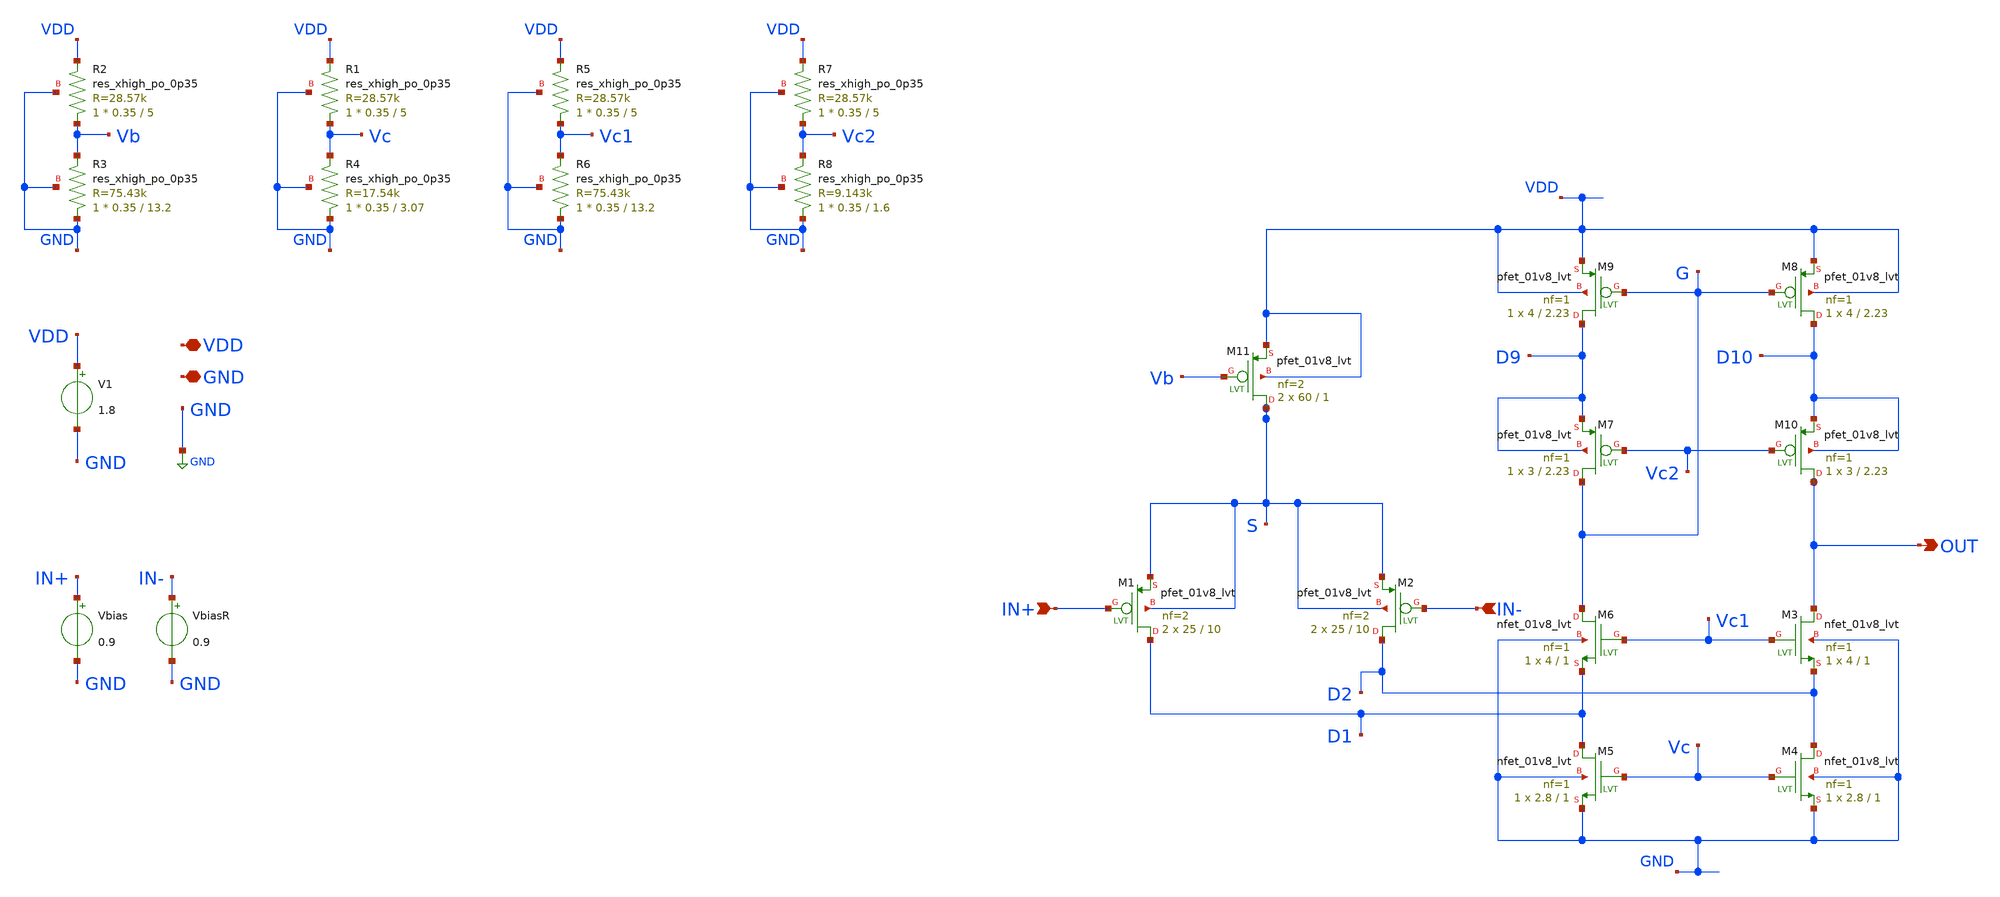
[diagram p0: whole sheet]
** sch_path: xschem/untitled-4.sch
**.subckt untitled-4 VDD GND IN+ IN- OUT
*.iopin VDD
*.iopin GND
*.ipin IN+
*.ipin IN-
*.opin OUT
V1 VDD GND 1.8
Vbias IN+ GND 0.9
XM11 S Vb VDD VDD sky130_fd_pr__pfet_01v8_lvt L=1 W=60 nf=2 ad='int((nf+1)/2) * W/nf * 0.29' as='int((nf+2)/2) * W/nf * 0.29'
+ pd='2*int((nf+1)/2) * (W/nf + 0.29)' ps='2*int((nf+2)/2) * (W/nf + 0.29)' nrd='0.29 / W' nrs='0.29 / W'
+ sa=0 sb=0 sd=0 mult=2 m=2
XM1 D1 IN+ S S sky130_fd_pr__pfet_01v8_lvt L=10 W=25 nf=2 ad='int((nf+1)/2) * W/nf * 0.29' as='int((nf+2)/2) * W/nf * 0.29'
+ pd='2*int((nf+1)/2) * (W/nf + 0.29)' ps='2*int((nf+2)/2) * (W/nf + 0.29)' nrd='0.29 / W' nrs='0.29 / W'
+ sa=0 sb=0 sd=0 mult=2 m=2
XM2 D2 IN- S S sky130_fd_pr__pfet_01v8_lvt L=10 W=25 nf=2 ad='int((nf+1)/2) * W/nf * 0.29' as='int((nf+2)/2) * W/nf * 0.29'
+ pd='2*int((nf+1)/2) * (W/nf + 0.29)' ps='2*int((nf+2)/2) * (W/nf + 0.29)' nrd='0.29 / W' nrs='0.29 / W'
+ sa=0 sb=0 sd=0 mult=2 m=2
XM3 OUT Vc1 D2 GND sky130_fd_pr__nfet_01v8_lvt L=1 W=4 nf=1 ad='int((nf+1)/2) * W/nf * 0.29' as='int((nf+2)/2) * W/nf * 0.29'
+ pd='2*int((nf+1)/2) * (W/nf + 0.29)' ps='2*int((nf+2)/2) * (W/nf + 0.29)' nrd='0.29 / W' nrs='0.29 / W'
+ sa=0 sb=0 sd=0 mult=1 m=1
XM4 D2 Vc GND GND sky130_fd_pr__nfet_01v8_lvt L=1 W=2.8 nf=1 ad='int((nf+1)/2) * W/nf * 0.29' as='int((nf+2)/2) * W/nf * 0.29'
+ pd='2*int((nf+1)/2) * (W/nf + 0.29)' ps='2*int((nf+2)/2) * (W/nf + 0.29)' nrd='0.29 / W' nrs='0.29 / W'
+ sa=0 sb=0 sd=0 mult=1 m=1
XM5 D1 Vc GND GND sky130_fd_pr__nfet_01v8_lvt L=1 W=2.8 nf=1 ad='int((nf+1)/2) * W/nf * 0.29' as='int((nf+2)/2) * W/nf * 0.29'
+ pd='2*int((nf+1)/2) * (W/nf + 0.29)' ps='2*int((nf+2)/2) * (W/nf + 0.29)' nrd='0.29 / W' nrs='0.29 / W'
+ sa=0 sb=0 sd=0 mult=1 m=1
XM6 G Vc1 D1 GND sky130_fd_pr__nfet_01v8_lvt L=1 W=4 nf=1 ad='int((nf+1)/2) * W/nf * 0.29' as='int((nf+2)/2) * W/nf * 0.29'
+ pd='2*int((nf+1)/2) * (W/nf + 0.29)' ps='2*int((nf+2)/2) * (W/nf + 0.29)' nrd='0.29 / W' nrs='0.29 / W'
+ sa=0 sb=0 sd=0 mult=1 m=1
XM7 G Vc2 D9 D9 sky130_fd_pr__pfet_01v8_lvt L=2.23 W=3 nf=1 ad='int((nf+1)/2) * W/nf * 0.29' as='int((nf+2)/2) * W/nf * 0.29'
+ pd='2*int((nf+1)/2) * (W/nf + 0.29)' ps='2*int((nf+2)/2) * (W/nf + 0.29)' nrd='0.29 / W' nrs='0.29 / W'
+ sa=0 sb=0 sd=0 mult=1 m=1
XM9 D9 G VDD VDD sky130_fd_pr__pfet_01v8_lvt L=2.23 W=4 nf=1 ad='int((nf+1)/2) * W/nf * 0.29' as='int((nf+2)/2) * W/nf * 0.29'
+ pd='2*int((nf+1)/2) * (W/nf + 0.29)' ps='2*int((nf+2)/2) * (W/nf + 0.29)' nrd='0.29 / W' nrs='0.29 / W'
+ sa=0 sb=0 sd=0 mult=1 m=1
XM8 D10 G VDD VDD sky130_fd_pr__pfet_01v8_lvt L=2.23 W=4 nf=1 ad='int((nf+1)/2) * W/nf * 0.29' as='int((nf+2)/2) * W/nf * 0.29'
+ pd='2*int((nf+1)/2) * (W/nf + 0.29)' ps='2*int((nf+2)/2) * (W/nf + 0.29)' nrd='0.29 / W' nrs='0.29 / W'
+ sa=0 sb=0 sd=0 mult=1 m=1
XM10 OUT Vc2 D10 D10 sky130_fd_pr__pfet_01v8_lvt L=2.23 W=3 nf=1 ad='int((nf+1)/2) * W/nf * 0.29' as='int((nf+2)/2) * W/nf * 0.29'
+ pd='2*int((nf+1)/2) * (W/nf + 0.29)' ps='2*int((nf+2)/2) * (W/nf + 0.29)' nrd='0.29 / W' nrs='0.29 / W'
+ sa=0 sb=0 sd=0 mult=1 m=1
XR2 Vb VDD GND sky130_fd_pr__res_xhigh_po_0p35 L=5 mult=1 m=1
XR3 GND Vb GND sky130_fd_pr__res_xhigh_po_0p35 L=13.2 mult=1 m=1
XR1 Vc VDD GND sky130_fd_pr__res_xhigh_po_0p35 L=5 mult=1 m=1
XR4 GND Vc GND sky130_fd_pr__res_xhigh_po_0p35 L=3.07 mult=1 m=1
XR5 Vc1 VDD GND sky130_fd_pr__res_xhigh_po_0p35 L=5 mult=1 m=1
XR6 GND Vc1 GND sky130_fd_pr__res_xhigh_po_0p35 L=13.2 mult=1 m=1
XR7 Vc2 VDD GND sky130_fd_pr__res_xhigh_po_0p35 L=5 mult=1 m=1
XR8 GND Vc2 GND sky130_fd_pr__res_xhigh_po_0p35 L=1.6 mult=1 m=1
VbiasR IN- GND 0.9
**** begin user architecture code



.control
    set wr_vecnames
    set wr_singlescale

    * Definiamo 3 scenari PVT
    let pvt_runs = 3
    let run = 1

    dowhile run <= pvt_runs
        if run == 1
            echo *SCENARIO 1: TYPICAL (27C, VDD 1.8V)
            set temp = 27
            alter VDD 1.8
        end
        if run == 2
            echo *CENARIO 2: HOT & LOW VOLTAGE (125C, VDD 1.62V)
            set temp = 125
            alter VDD 1.62
        end
        if run == 3
            echo *SCENARIO 3: COLD & HIGH VOLTAGE (-40C, VDD 1.98V)
            set temp = -40
            alter VDD 1.98
        end

        * Esecuzione analisi DC
        dc Vbias 0.8 1 0.001

        let run = run + 1
    end

    * --- PLOT RISULTATI ---

    * Visualizzazione della curva di trasferimento DC
    plot dc1.v(OUT) dc2.v(OUT) dc3.v(OUT) title 'DC Transfer PVT'

    * Visualizzazione del Guadagno (Derivata)
    * Nota: con l'impedenza di 3Mohm, vedrai i picchi spostarsi e cambiare altezza
    plot deriv(dc1.v(out)) deriv(dc2.v(out)) deriv(dc3.v(out)) title 'DC Gain PVT'

.endc


.lib $::SKYWATER_MODELS/sky130.lib.spice tt
**** end user architecture code
**.ends
.GLOBAL GND
.end
